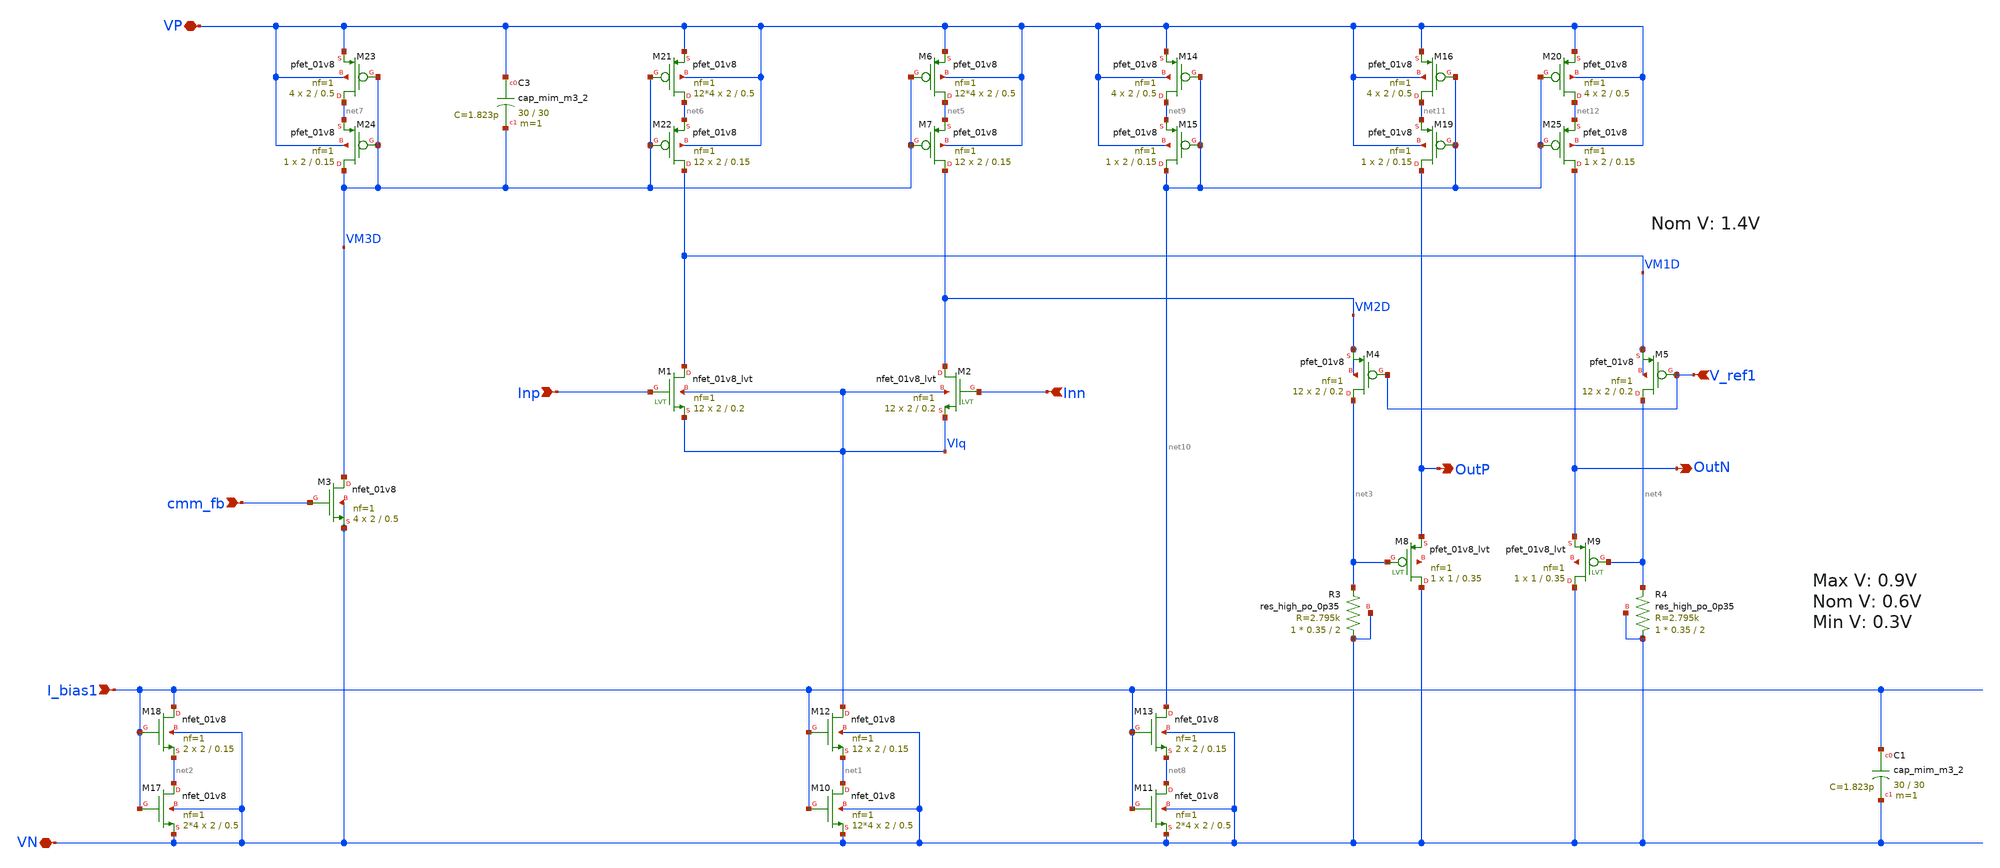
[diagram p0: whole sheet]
** sch_path: xschem/comp/comp_casc2.sch
**.subckt comp_casc2 Inp I_bias1 Inn VP VN OutN OutP V_ref1 cmm_fb
*.ipin Inp
*.ipin I_bias1
*.ipin Inn
*.iopin VP
*.iopin VN
*.opin OutN
*.opin OutP
*.ipin V_ref1
*.ipin cmm_fb
XM1 VM1D Inp VIq VIq sky130_fd_pr__nfet_01v8_lvt L=0.2 W=2 nf=1 ad='int((nf+1)/2) * W/nf * 0.29' as='int((nf+2)/2) * W/nf * 0.29'
+ pd='2*int((nf+1)/2) * (W/nf + 0.29)' ps='2*int((nf+2)/2) * (W/nf + 0.29)' nrd='0.29 / W' nrs='0.29 / W'
+ sa=0 sb=0 sd=0 mult=12 m=12
XM2 VM2D Inn VIq VIq sky130_fd_pr__nfet_01v8_lvt L=0.2 W=2 nf=1 ad='int((nf+1)/2) * W/nf * 0.29' as='int((nf+2)/2) * W/nf * 0.29'
+ pd='2*int((nf+1)/2) * (W/nf + 0.29)' ps='2*int((nf+2)/2) * (W/nf + 0.29)' nrd='0.29 / W' nrs='0.29 / W'
+ sa=0 sb=0 sd=0 mult=12 m=12
XM10 net1 I_bias1 VN VN sky130_fd_pr__nfet_01v8 L=0.5 W=2 nf=1 ad='int((nf+1)/2) * W/nf * 0.29' as='int((nf+2)/2) * W/nf * 0.29'
+ pd='2*int((nf+1)/2) * (W/nf + 0.29)' ps='2*int((nf+2)/2) * (W/nf + 0.29)' nrd='0.29 / W' nrs='0.29 / W'
+ sa=0 sb=0 sd=0 mult=12*4 m=12*4
XM12 VIq I_bias1 net1 VN sky130_fd_pr__nfet_01v8 L=0.15 W=2 nf=1 ad='int((nf+1)/2) * W/nf * 0.29' as='int((nf+2)/2) * W/nf * 0.29'
+ pd='2*int((nf+1)/2) * (W/nf + 0.29)' ps='2*int((nf+2)/2) * (W/nf + 0.29)' nrd='0.29 / W' nrs='0.29 / W'
+ sa=0 sb=0 sd=0 mult=12 m=12
XM17 net2 I_bias1 VN VN sky130_fd_pr__nfet_01v8 L=0.5 W=2 nf=1 ad='int((nf+1)/2) * W/nf * 0.29' as='int((nf+2)/2) * W/nf * 0.29'
+ pd='2*int((nf+1)/2) * (W/nf + 0.29)' ps='2*int((nf+2)/2) * (W/nf + 0.29)' nrd='0.29 / W' nrs='0.29 / W'
+ sa=0 sb=0 sd=0 mult=2*4 m=2*4
XM18 I_bias1 I_bias1 net2 VN sky130_fd_pr__nfet_01v8 L=0.15 W=2 nf=1 ad='int((nf+1)/2) * W/nf * 0.29'
+ as='int((nf+2)/2) * W/nf * 0.29' pd='2*int((nf+1)/2) * (W/nf + 0.29)' ps='2*int((nf+2)/2) * (W/nf + 0.29)'
+ nrd='0.29 / W' nrs='0.29 / W' sa=0 sb=0 sd=0 mult=2 m=2
XC1 I_bias1 VN sky130_fd_pr__cap_mim_m3_2 W=30 L=30 MF=1 m=1
XM4 net3 V_ref1 VM2D VM2D sky130_fd_pr__pfet_01v8 L=0.2 W=2 nf=1 ad='int((nf+1)/2) * W/nf * 0.29' as='int((nf+2)/2) * W/nf * 0.29'
+ pd='2*int((nf+1)/2) * (W/nf + 0.29)' ps='2*int((nf+2)/2) * (W/nf + 0.29)' nrd='0.29 / W' nrs='0.29 / W'
+ sa=0 sb=0 sd=0 mult=12 m=12
XR3 VN net3 VN sky130_fd_pr__res_high_po_0p35 L=2 mult=1 m=1
XR4 VN net4 VN sky130_fd_pr__res_high_po_0p35 L=2 mult=1 m=1
XM5 net4 V_ref1 VM1D VM1D sky130_fd_pr__pfet_01v8 L=0.2 W=2 nf=1 ad='int((nf+1)/2) * W/nf * 0.29' as='int((nf+2)/2) * W/nf * 0.29'
+ pd='2*int((nf+1)/2) * (W/nf + 0.29)' ps='2*int((nf+2)/2) * (W/nf + 0.29)' nrd='0.29 / W' nrs='0.29 / W'
+ sa=0 sb=0 sd=0 mult=12 m=12
XM21 net6 VM3D VP VP sky130_fd_pr__pfet_01v8 L=0.5 W=2 nf=1 ad='int((nf+1)/2) * W/nf * 0.29' as='int((nf+2)/2) * W/nf * 0.29'
+ pd='2*int((nf+1)/2) * (W/nf + 0.29)' ps='2*int((nf+2)/2) * (W/nf + 0.29)' nrd='0.29 / W' nrs='0.29 / W'
+ sa=0 sb=0 sd=0 mult=12*4 m=12*4
XM22 VM1D VM3D net6 VP sky130_fd_pr__pfet_01v8 L=0.15 W=2 nf=1 ad='int((nf+1)/2) * W/nf * 0.29' as='int((nf+2)/2) * W/nf * 0.29'
+ pd='2*int((nf+1)/2) * (W/nf + 0.29)' ps='2*int((nf+2)/2) * (W/nf + 0.29)' nrd='0.29 / W' nrs='0.29 / W'
+ sa=0 sb=0 sd=0 mult=12 m=12
XM23 net7 VM3D VP VP sky130_fd_pr__pfet_01v8 L=0.5 W=2 nf=1 ad='int((nf+1)/2) * W/nf * 0.29' as='int((nf+2)/2) * W/nf * 0.29'
+ pd='2*int((nf+1)/2) * (W/nf + 0.29)' ps='2*int((nf+2)/2) * (W/nf + 0.29)' nrd='0.29 / W' nrs='0.29 / W'
+ sa=0 sb=0 sd=0 mult=4 m=4
XM24 VM3D VM3D net7 VP sky130_fd_pr__pfet_01v8 L=0.15 W=2 nf=1 ad='int((nf+1)/2) * W/nf * 0.29' as='int((nf+2)/2) * W/nf * 0.29'
+ pd='2*int((nf+1)/2) * (W/nf + 0.29)' ps='2*int((nf+2)/2) * (W/nf + 0.29)' nrd='0.29 / W' nrs='0.29 / W'
+ sa=0 sb=0 sd=0 mult=1 m=1
XC3 VP VM3D sky130_fd_pr__cap_mim_m3_2 W=30 L=30 MF=1 m=1
XM3 VM3D cmm_fb VN VN sky130_fd_pr__nfet_01v8 L=0.5 W=2 nf=1 ad='int((nf+1)/2) * W/nf * 0.29' as='int((nf+2)/2) * W/nf * 0.29'
+ pd='2*int((nf+1)/2) * (W/nf + 0.29)' ps='2*int((nf+2)/2) * (W/nf + 0.29)' nrd='0.29 / W' nrs='0.29 / W'
+ sa=0 sb=0 sd=0 mult=4 m=4
XM6 net5 VM3D VP VP sky130_fd_pr__pfet_01v8 L=0.5 W=2 nf=1 ad='int((nf+1)/2) * W/nf * 0.29' as='int((nf+2)/2) * W/nf * 0.29'
+ pd='2*int((nf+1)/2) * (W/nf + 0.29)' ps='2*int((nf+2)/2) * (W/nf + 0.29)' nrd='0.29 / W' nrs='0.29 / W'
+ sa=0 sb=0 sd=0 mult=12*4 m=12*4
XM7 VM2D VM3D net5 VP sky130_fd_pr__pfet_01v8 L=0.15 W=2 nf=1 ad='int((nf+1)/2) * W/nf * 0.29' as='int((nf+2)/2) * W/nf * 0.29'
+ pd='2*int((nf+1)/2) * (W/nf + 0.29)' ps='2*int((nf+2)/2) * (W/nf + 0.29)' nrd='0.29 / W' nrs='0.29 / W'
+ sa=0 sb=0 sd=0 mult=12 m=12
XM8 VN net3 OutP net13 sky130_fd_pr__pfet_01v8_lvt L=0.35 W=1 nf=1 ad='int((nf+1)/2) * W/nf * 0.29' as='int((nf+2)/2) * W/nf * 0.29'
+ pd='2*int((nf+1)/2) * (W/nf + 0.29)' ps='2*int((nf+2)/2) * (W/nf + 0.29)' nrd='0.29 / W' nrs='0.29 / W'
+ sa=0 sb=0 sd=0 mult=1 m=1
XM9 VN net4 OutN net14 sky130_fd_pr__pfet_01v8_lvt L=0.35 W=1 nf=1 ad='int((nf+1)/2) * W/nf * 0.29' as='int((nf+2)/2) * W/nf * 0.29'
+ pd='2*int((nf+1)/2) * (W/nf + 0.29)' ps='2*int((nf+2)/2) * (W/nf + 0.29)' nrd='0.29 / W' nrs='0.29 / W'
+ sa=0 sb=0 sd=0 mult=1 m=1
XM11 net8 I_bias1 VN VN sky130_fd_pr__nfet_01v8 L=0.5 W=2 nf=1 ad='int((nf+1)/2) * W/nf * 0.29' as='int((nf+2)/2) * W/nf * 0.29'
+ pd='2*int((nf+1)/2) * (W/nf + 0.29)' ps='2*int((nf+2)/2) * (W/nf + 0.29)' nrd='0.29 / W' nrs='0.29 / W'
+ sa=0 sb=0 sd=0 mult=2*4 m=2*4
XM13 net10 I_bias1 net8 VN sky130_fd_pr__nfet_01v8 L=0.15 W=2 nf=1 ad='int((nf+1)/2) * W/nf * 0.29' as='int((nf+2)/2) * W/nf * 0.29'
+ pd='2*int((nf+1)/2) * (W/nf + 0.29)' ps='2*int((nf+2)/2) * (W/nf + 0.29)' nrd='0.29 / W' nrs='0.29 / W'
+ sa=0 sb=0 sd=0 mult=2 m=2
XM14 net9 net10 VP VP sky130_fd_pr__pfet_01v8 L=0.5 W=2 nf=1 ad='int((nf+1)/2) * W/nf * 0.29' as='int((nf+2)/2) * W/nf * 0.29'
+ pd='2*int((nf+1)/2) * (W/nf + 0.29)' ps='2*int((nf+2)/2) * (W/nf + 0.29)' nrd='0.29 / W' nrs='0.29 / W'
+ sa=0 sb=0 sd=0 mult=4 m=4
XM15 net10 net10 net9 VP sky130_fd_pr__pfet_01v8 L=0.15 W=2 nf=1 ad='int((nf+1)/2) * W/nf * 0.29' as='int((nf+2)/2) * W/nf * 0.29'
+ pd='2*int((nf+1)/2) * (W/nf + 0.29)' ps='2*int((nf+2)/2) * (W/nf + 0.29)' nrd='0.29 / W' nrs='0.29 / W'
+ sa=0 sb=0 sd=0 mult=1 m=1
XM16 net11 net10 VP VP sky130_fd_pr__pfet_01v8 L=0.5 W=2 nf=1 ad='int((nf+1)/2) * W/nf * 0.29' as='int((nf+2)/2) * W/nf * 0.29'
+ pd='2*int((nf+1)/2) * (W/nf + 0.29)' ps='2*int((nf+2)/2) * (W/nf + 0.29)' nrd='0.29 / W' nrs='0.29 / W'
+ sa=0 sb=0 sd=0 mult=4 m=4
XM19 OutP net10 net11 VP sky130_fd_pr__pfet_01v8 L=0.15 W=2 nf=1 ad='int((nf+1)/2) * W/nf * 0.29' as='int((nf+2)/2) * W/nf * 0.29'
+ pd='2*int((nf+1)/2) * (W/nf + 0.29)' ps='2*int((nf+2)/2) * (W/nf + 0.29)' nrd='0.29 / W' nrs='0.29 / W'
+ sa=0 sb=0 sd=0 mult=1 m=1
XM20 net12 net10 VP VP sky130_fd_pr__pfet_01v8 L=0.5 W=2 nf=1 ad='int((nf+1)/2) * W/nf * 0.29' as='int((nf+2)/2) * W/nf * 0.29'
+ pd='2*int((nf+1)/2) * (W/nf + 0.29)' ps='2*int((nf+2)/2) * (W/nf + 0.29)' nrd='0.29 / W' nrs='0.29 / W'
+ sa=0 sb=0 sd=0 mult=4 m=4
XM25 OutN net10 net12 VP sky130_fd_pr__pfet_01v8 L=0.15 W=2 nf=1 ad='int((nf+1)/2) * W/nf * 0.29' as='int((nf+2)/2) * W/nf * 0.29'
+ pd='2*int((nf+1)/2) * (W/nf + 0.29)' ps='2*int((nf+2)/2) * (W/nf + 0.29)' nrd='0.29 / W' nrs='0.29 / W'
+ sa=0 sb=0 sd=0 mult=1 m=1
**** begin user architecture code

*.lib $::SKYWATER_MODELS/sky130.lib.spice tt
.lib $::SKYWATER_MODELS/sky130.lib.spice.tt.red tt



*.options savecurrents
.option warn=1
.control
set wr_vecnames
set wr_singlescale
* Power consumption
op
* save all
* #OP#
print @m.xm1.msky130_fd_pr__nfet_01v8_lvt[gds]
print vdd#branch
print v(vm2d)
print v(vm3d)
print v(UD_M5)
wrdata 'result_op.csv' vdd#branch
ac dec 10 1 10G
meas ac dc_gain_vm2d FIND vdb(vm2d) AT=1
let bw_amp_vm2d=dc_gain_vm2d-3
meas ac dc_gain_vm3d FIND vdb(vm3d) AT=1
let bw_amp_vm3d=dc_gain_vm3d-3
meas ac bw_vm2d when vdb(vm2d)=bw_amp_vm2d
meas ac bw_vm3d when vdb(vm3d)=bw_amp_vm3d
*MEAS AC phasem FIND vp(vm2d) WHEN vdb(vm2d)=0
* wrdata 'result_ac.csv' dc_gain bw
* plot vdb(vm2D) log
*
*print WM3D
run
reset
save @m.xm1.msky130_fd_pr__nfet_01v8_lvt[gds]
save @m.xm1.msky130_fd_pr__nfet_01v8_lvt[gm]
save @m.xm1.msky130_fd_pr__nfet_01v8_lvt[cgs]
save @m.xm1.msky130_fd_pr__nfet_01v8_lvt[cdg]
save @m.xm2.msky130_fd_pr__nfet_01v8_lvt[gm]
save @m.xm2.msky130_fd_pr__nfet_01v8_lvt[gds]
save @m.xm2.msky130_fd_pr__nfet_01v8_lvt[cgs]
save @m.xm2.msky130_fd_pr__nfet_01v8_lvt[cdg]
save @m.xm3.msky130_fd_pr__nfet_01v8_lvt[gm]
save @m.xm3.msky130_fd_pr__nfet_01v8_lvt[gds]
save @m.xm3.msky130_fd_pr__nfet_01v8_lvt[cgs]
save @m.xm3.msky130_fd_pr__nfet_01v8_lvt[cdg]
save @m.xm4.msky130_fd_pr__nfet_01v8_lvt[gm]
save @m.xm4.msky130_fd_pr__nfet_01v8_lvt[gds]
save @m.xm4.msky130_fd_pr__nfet_01v8_lvt[cgs]
save @m.xm4.msky130_fd_pr__nfet_01v8_lvt[cdg]
save @m.xm5.msky130_fd_pr__pfet_01v8_lvt[gm]
save @m.xm5.msky130_fd_pr__pfet_01v8_lvt[gds]
save @m.xm5.msky130_fd_pr__pfet_01v8_lvt[cgs]
save @m.xm5.msky130_fd_pr__pfet_01v8_lvt[cdg]
save @m.xm6.msky130_fd_pr__pfet_01v8_lvt[gm]
save @m.xm6.msky130_fd_pr__pfet_01v8_lvt[gds]
save @m.xm6.msky130_fd_pr__pfet_01v8_lvt[cgs]
save @m.xm6.msky130_fd_pr__pfet_01v8_lvt[cdg]
save @m.xm7.msky130_fd_pr__nfet_01v8_lvt[gm]
save @m.xm7.msky130_fd_pr__nfet_01v8_lvt[gds]
save @m.xm7.msky130_fd_pr__nfet_01v8_lvt[cgs]
save @m.xm7.msky130_fd_pr__nfet_01v8_lvt[cdg]
save @m.xm8.msky130_fd_pr__nfet_01v8_lvt[gm]
save @m.xm8.msky130_fd_pr__nfet_01v8_lvt[gds]
save @m.xm8.msky130_fd_pr__nfet_01v8_lvt[cgs]
save @m.xm8.msky130_fd_pr__nfet_01v8_lvt[cdg]
save @m.xm9.msky130_fd_pr__nfet_01v8_lvt[gm]
save @m.xm9.msky130_fd_pr__nfet_01v8_lvt[gds]
save @m.xm9.msky130_fd_pr__nfet_01v8_lvt[cgs]
save @m.xm9.msky130_fd_pr__nfet_01v8_lvt[cdg]
save v(Voutp)
save v(Voutn)
save v(VIa)
save v(VIq)

save v(Vinn)
save v(Vinp)
save v(VM8G)

op
write comp.raw
run
*reset
*noise v(vm1d) I1 dec 100 1 10G
*print all
*setplot noise2
*write noise2.raw
*run
reset
ac dec 10 1 1T
plot vdb(Voutp) vdb(Voutn)
plot phase(Voutp)/pi*180 phase(Voutn)/pi*180
run
reset
tran 1ps 10ns
plot v(Vinp) v(Voutn) v(Voutp)
run
.endc


**** end user architecture code
**.ends
.end
